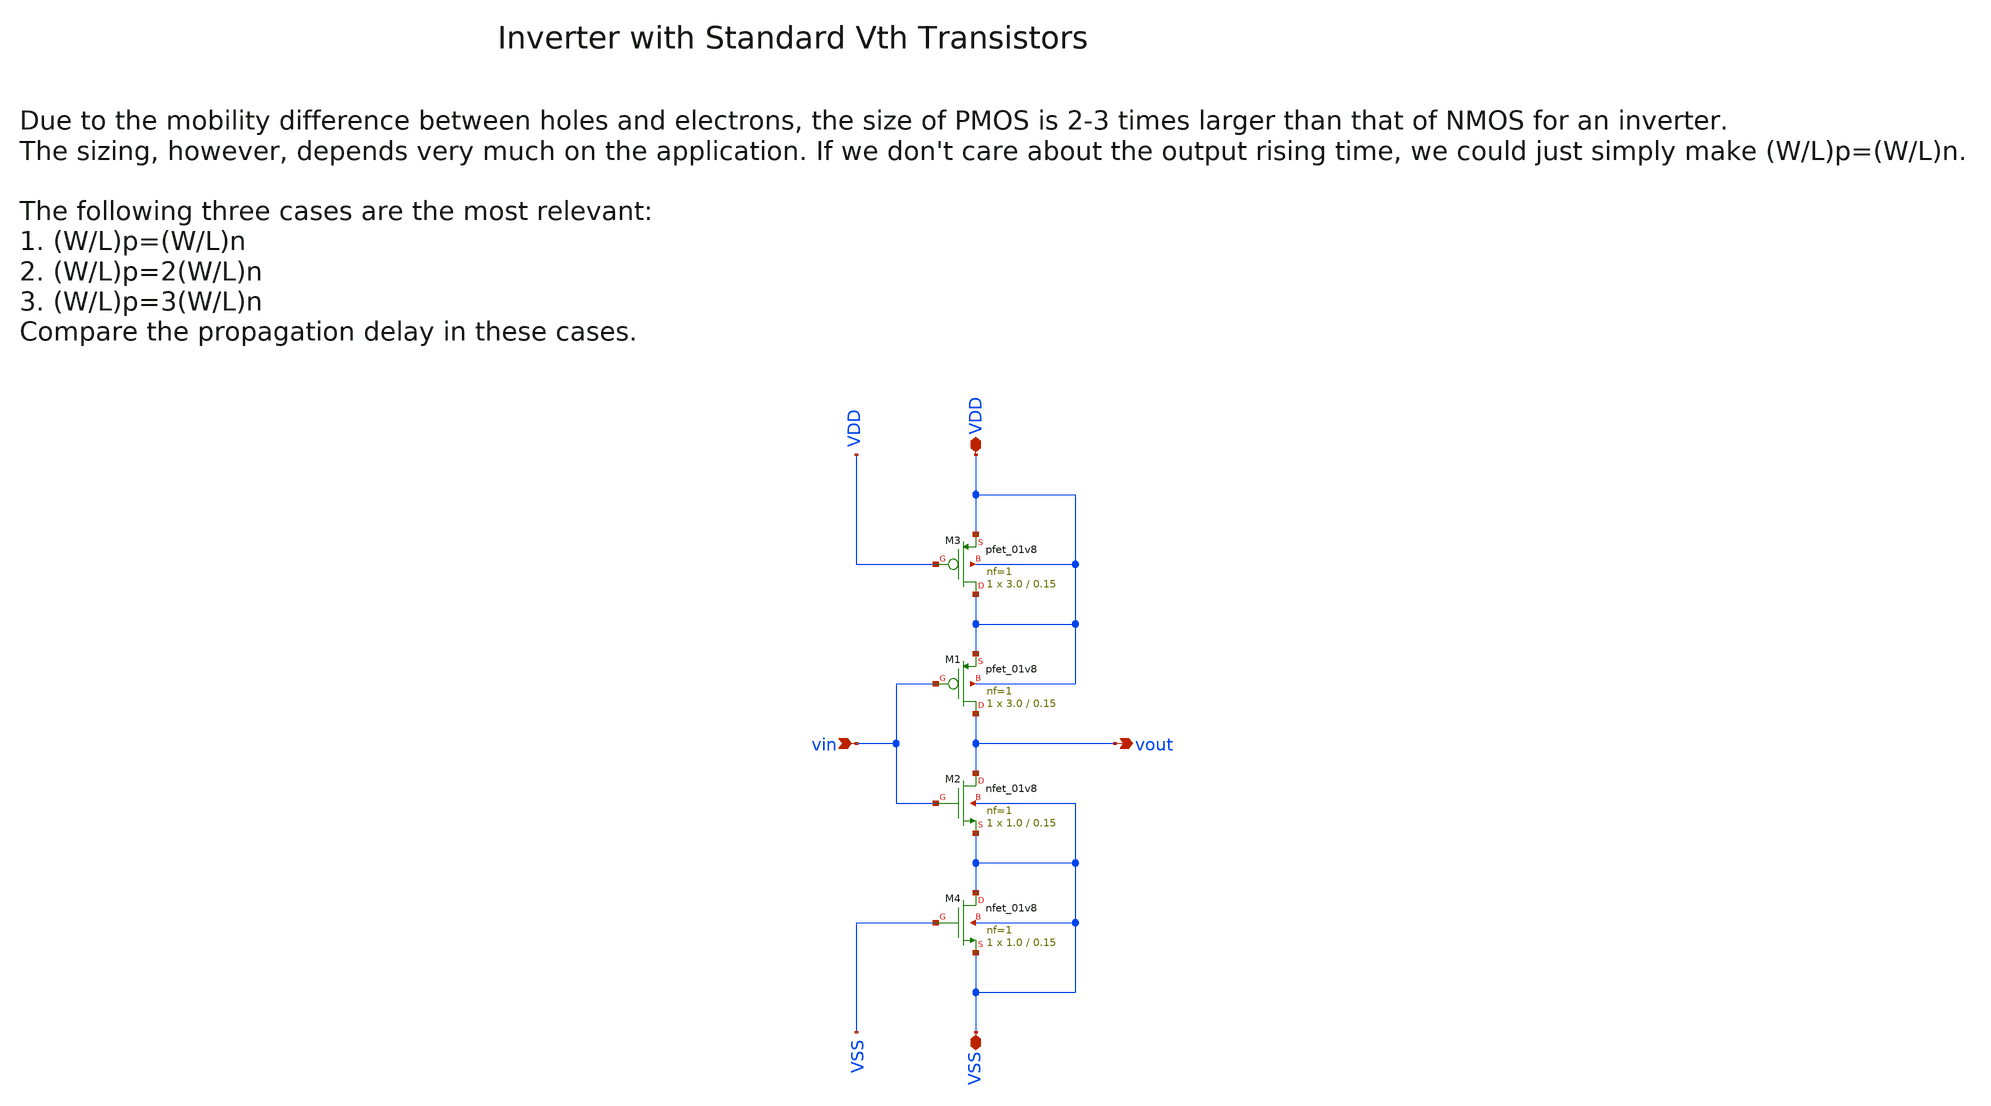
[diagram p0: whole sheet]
** sch_path: sky130/macros/iqmod/schematic/wspr_tx_iqmod_mixer_lo_logic_inv_NF1.sch
**.subckt wspr_tx_iqmod_mixer_lo_logic_inv_NF1 vin VDD VSS vout
*.ipin vin
*.iopin VDD
*.iopin VSS
*.opin vout
XM1 vout vin VDD VDD sky130_fd_pr__pfet_01v8 L=0.15 W=3.0 nf=1 ad='int((1 + 1)/2) * 3.0 / 1 * 0.29' as='int((1 + 2)/2) * 3.0 / 1 * 0.29'
+ pd='2*int((1 + 1)/2) * (3.0 / 1 + 0.29)' ps='2*int((1 + 2)/2) * (3.0 / 1 + 0.29)' nrd='0.29 / 3.0 ' nrs='0.29 / 3.0 '
+ sa=0 sb=0 sd=0 mult=1 m=1
XM3 VDD VDD VDD VDD sky130_fd_pr__pfet_01v8 L=0.15 W=3.0 nf=1 ad='int((1 + 1)/2) * 3.0 / 1 * 0.29' as='int((1 + 2)/2) * 3.0 / 1 * 0.29'
+ pd='2*int((1 + 1)/2) * (3.0 / 1 + 0.29)' ps='2*int((1 + 2)/2) * (3.0 / 1 + 0.29)' nrd='0.29 / 3.0 ' nrs='0.29 / 3.0 '
+ sa=0 sb=0 sd=0 mult=1 m=1
XM2 vout vin VSS VSS sky130_fd_pr__nfet_01v8 L=0.15 W=1.0 nf=1 ad='int((1 + 1)/2) * 1.0 / 1 * 0.29' as='int((1 + 2)/2) * 1.0 / 1 * 0.29'
+ pd='2*int((1 + 1)/2) * (1.0 / 1 + 0.29)' ps='2*int((1 + 2)/2) * (1.0 / 1 + 0.29)' nrd='0.29 / 1.0 ' nrs='0.29 / 1.0 '
+ sa=0 sb=0 sd=0 mult=1 m=1
XM4 VSS VSS VSS VSS sky130_fd_pr__nfet_01v8 L=0.15 W=1.0 nf=1 ad='int((1 + 1)/2) * 1.0 / 1 * 0.29' as='int((1 + 2)/2) * 1.0 / 1 * 0.29'
+ pd='2*int((1 + 1)/2) * (1.0 / 1 + 0.29)' ps='2*int((1 + 2)/2) * (1.0 / 1 + 0.29)' nrd='0.29 / 1.0 ' nrs='0.29 / 1.0 '
+ sa=0 sb=0 sd=0 mult=1 m=1
**.ends
.end
